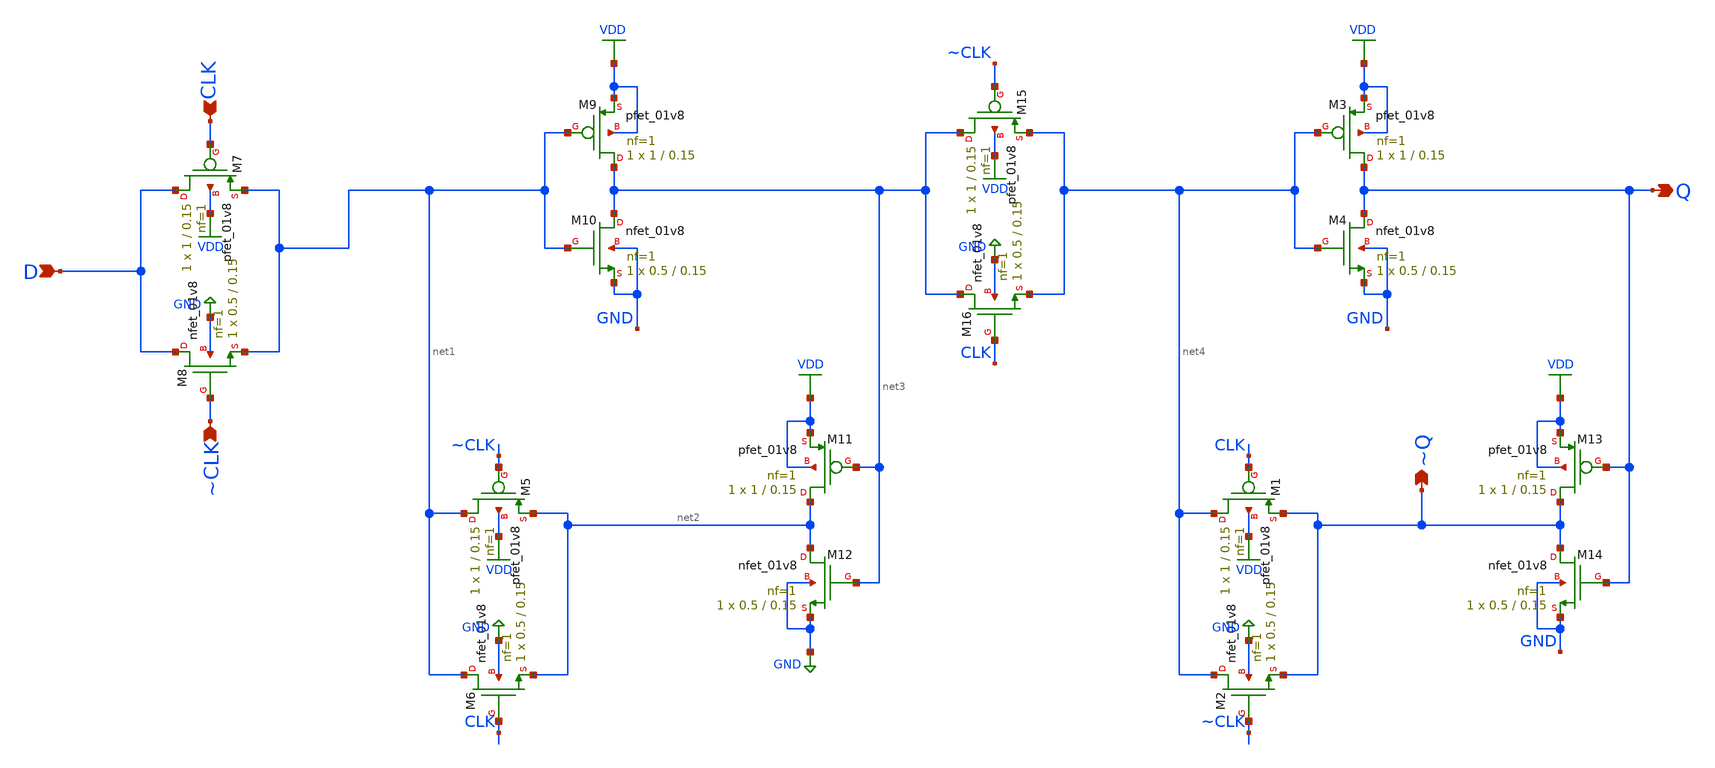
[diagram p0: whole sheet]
** sch_path: xschem/dff.sch
**.subckt dff D ~CLK CLK ~Q Q
*.ipin D
*.ipin ~CLK
*.ipin CLK
*.opin ~Q
*.opin Q
XM5 net1 ~CLK net2 VDD sky130_fd_pr__pfet_01v8 L=0.15 W=1 nf=1 ad='int((nf+1)/2) * W/nf * 0.29' as='int((nf+2)/2) * W/nf * 0.29'
+ pd='2*int((nf+1)/2) * (W/nf + 0.29)' ps='2*int((nf+2)/2) * (W/nf + 0.29)' nrd='0.29 / W' nrs='0.29 / W'
+ sa=0 sb=0 sd=0 mult=1 m=1
XM6 net1 CLK net2 GND sky130_fd_pr__nfet_01v8 L=0.15 W=0.5 nf=1 ad='int((nf+1)/2) * W/nf * 0.29' as='int((nf+2)/2) * W/nf * 0.29'
+ pd='2*int((nf+1)/2) * (W/nf + 0.29)' ps='2*int((nf+2)/2) * (W/nf + 0.29)' nrd='0.29 / W' nrs='0.29 / W'
+ sa=0 sb=0 sd=0 mult=1 m=1
XM7 D CLK net1 VDD sky130_fd_pr__pfet_01v8 L=0.15 W=1 nf=1 ad='int((nf+1)/2) * W/nf * 0.29' as='int((nf+2)/2) * W/nf * 0.29'
+ pd='2*int((nf+1)/2) * (W/nf + 0.29)' ps='2*int((nf+2)/2) * (W/nf + 0.29)' nrd='0.29 / W' nrs='0.29 / W'
+ sa=0 sb=0 sd=0 mult=1 m=1
XM8 D ~CLK net1 GND sky130_fd_pr__nfet_01v8 L=0.15 W=0.5 nf=1 ad='int((nf+1)/2) * W/nf * 0.29' as='int((nf+2)/2) * W/nf * 0.29'
+ pd='2*int((nf+1)/2) * (W/nf + 0.29)' ps='2*int((nf+2)/2) * (W/nf + 0.29)' nrd='0.29 / W' nrs='0.29 / W'
+ sa=0 sb=0 sd=0 mult=1 m=1
XM9 net3 net1 VDD VDD sky130_fd_pr__pfet_01v8 L=0.15 W=1 nf=1 ad='int((nf+1)/2) * W/nf * 0.29' as='int((nf+2)/2) * W/nf * 0.29'
+ pd='2*int((nf+1)/2) * (W/nf + 0.29)' ps='2*int((nf+2)/2) * (W/nf + 0.29)' nrd='0.29 / W' nrs='0.29 / W'
+ sa=0 sb=0 sd=0 mult=1 m=1
XM10 net3 net1 GND GND sky130_fd_pr__nfet_01v8 L=0.15 W=0.5 nf=1 ad='int((nf+1)/2) * W/nf * 0.29' as='int((nf+2)/2) * W/nf * 0.29'
+ pd='2*int((nf+1)/2) * (W/nf + 0.29)' ps='2*int((nf+2)/2) * (W/nf + 0.29)' nrd='0.29 / W' nrs='0.29 / W'
+ sa=0 sb=0 sd=0 mult=1 m=1
XM11 net2 net3 VDD VDD sky130_fd_pr__pfet_01v8 L=0.15 W=1 nf=1 ad='int((nf+1)/2) * W/nf * 0.29' as='int((nf+2)/2) * W/nf * 0.29'
+ pd='2*int((nf+1)/2) * (W/nf + 0.29)' ps='2*int((nf+2)/2) * (W/nf + 0.29)' nrd='0.29 / W' nrs='0.29 / W'
+ sa=0 sb=0 sd=0 mult=1 m=1
XM12 net2 net3 GND GND sky130_fd_pr__nfet_01v8 L=0.15 W=0.5 nf=1 ad='int((nf+1)/2) * W/nf * 0.29' as='int((nf+2)/2) * W/nf * 0.29'
+ pd='2*int((nf+1)/2) * (W/nf + 0.29)' ps='2*int((nf+2)/2) * (W/nf + 0.29)' nrd='0.29 / W' nrs='0.29 / W'
+ sa=0 sb=0 sd=0 mult=1 m=1
XM1 net4 CLK ~Q VDD sky130_fd_pr__pfet_01v8 L=0.15 W=1 nf=1 ad='int((nf+1)/2) * W/nf * 0.29' as='int((nf+2)/2) * W/nf * 0.29'
+ pd='2*int((nf+1)/2) * (W/nf + 0.29)' ps='2*int((nf+2)/2) * (W/nf + 0.29)' nrd='0.29 / W' nrs='0.29 / W'
+ sa=0 sb=0 sd=0 mult=1 m=1
XM2 net4 ~CLK ~Q GND sky130_fd_pr__nfet_01v8 L=0.15 W=0.5 nf=1 ad='int((nf+1)/2) * W/nf * 0.29' as='int((nf+2)/2) * W/nf * 0.29'
+ pd='2*int((nf+1)/2) * (W/nf + 0.29)' ps='2*int((nf+2)/2) * (W/nf + 0.29)' nrd='0.29 / W' nrs='0.29 / W'
+ sa=0 sb=0 sd=0 mult=1 m=1
XM3 Q net4 VDD VDD sky130_fd_pr__pfet_01v8 L=0.15 W=1 nf=1 ad='int((nf+1)/2) * W/nf * 0.29' as='int((nf+2)/2) * W/nf * 0.29'
+ pd='2*int((nf+1)/2) * (W/nf + 0.29)' ps='2*int((nf+2)/2) * (W/nf + 0.29)' nrd='0.29 / W' nrs='0.29 / W'
+ sa=0 sb=0 sd=0 mult=1 m=1
XM4 Q net4 GND GND sky130_fd_pr__nfet_01v8 L=0.15 W=0.5 nf=1 ad='int((nf+1)/2) * W/nf * 0.29' as='int((nf+2)/2) * W/nf * 0.29'
+ pd='2*int((nf+1)/2) * (W/nf + 0.29)' ps='2*int((nf+2)/2) * (W/nf + 0.29)' nrd='0.29 / W' nrs='0.29 / W'
+ sa=0 sb=0 sd=0 mult=1 m=1
XM13 ~Q Q VDD VDD sky130_fd_pr__pfet_01v8 L=0.15 W=1 nf=1 ad='int((nf+1)/2) * W/nf * 0.29' as='int((nf+2)/2) * W/nf * 0.29'
+ pd='2*int((nf+1)/2) * (W/nf + 0.29)' ps='2*int((nf+2)/2) * (W/nf + 0.29)' nrd='0.29 / W' nrs='0.29 / W'
+ sa=0 sb=0 sd=0 mult=1 m=1
XM14 ~Q Q GND GND sky130_fd_pr__nfet_01v8 L=0.15 W=0.5 nf=1 ad='int((nf+1)/2) * W/nf * 0.29' as='int((nf+2)/2) * W/nf * 0.29'
+ pd='2*int((nf+1)/2) * (W/nf + 0.29)' ps='2*int((nf+2)/2) * (W/nf + 0.29)' nrd='0.29 / W' nrs='0.29 / W'
+ sa=0 sb=0 sd=0 mult=1 m=1
XM15 net3 ~CLK net4 VDD sky130_fd_pr__pfet_01v8 L=0.15 W=1 nf=1 ad='int((nf+1)/2) * W/nf * 0.29' as='int((nf+2)/2) * W/nf * 0.29'
+ pd='2*int((nf+1)/2) * (W/nf + 0.29)' ps='2*int((nf+2)/2) * (W/nf + 0.29)' nrd='0.29 / W' nrs='0.29 / W'
+ sa=0 sb=0 sd=0 mult=1 m=1
XM16 net3 CLK net4 GND sky130_fd_pr__nfet_01v8 L=0.15 W=0.5 nf=1 ad='int((nf+1)/2) * W/nf * 0.29' as='int((nf+2)/2) * W/nf * 0.29'
+ pd='2*int((nf+1)/2) * (W/nf + 0.29)' ps='2*int((nf+2)/2) * (W/nf + 0.29)' nrd='0.29 / W' nrs='0.29 / W'
+ sa=0 sb=0 sd=0 mult=1 m=1
**.ends
.GLOBAL VDD
.GLOBAL GND
.end
